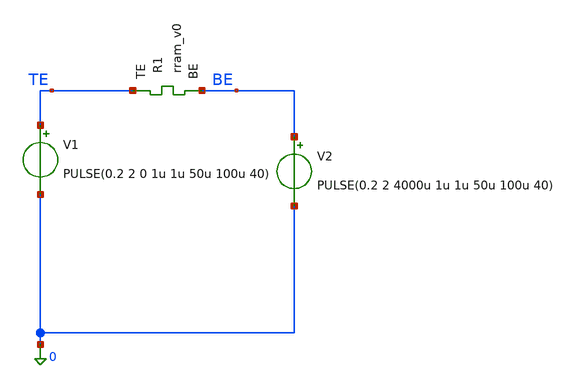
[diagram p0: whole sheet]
** sch_path: memristor_models/wellposed/tb_pulses_well.sch
**.subckt tb_pulses_well
V1 TE 0 PULSE(0.2 2 0 1u 1u 50u 100u 40)
V2 BE 0 PULSE(0.2 2 4000u 1u 1u 50u 100u 40)
XR1 TE BE rram_v0
**** begin user architecture code

** opencircuitdesign pdks install
.inc $::SKYWATER_MODELS/rram_v0.spice



.option savecurrents
.tran 1u 8m
.control
	save all
	run
	write tb_pulses_well.raw
.endc



**** end user architecture code
**.ends
.end
